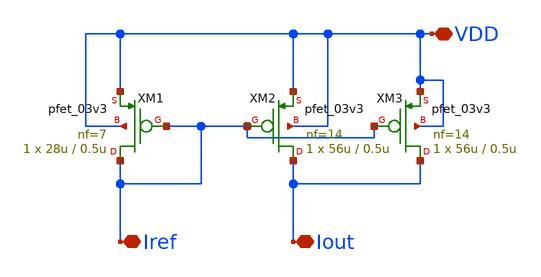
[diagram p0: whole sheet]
** sch_path: designs/mirrors/schematic/pmos_mirror.sch
**.subckt pmos_mirror VDD Iref Iout
*.iopin VDD
*.iopin Iref
*.iopin Iout
XM1 Iref Iref VDD VDD pfet_03v3 L=0.5u W=28u nf=7 ad='int((nf+1)/2) * W/nf * 0.18u' as='int((nf+2)/2) * W/nf * 0.18u'
+ pd='2*int((nf+1)/2) * (W/nf + 0.18u)' ps='2*int((nf+2)/2) * (W/nf + 0.18u)' nrd='0.18u / W' nrs='0.18u / W'
+ sa=0 sb=0 sd=0 m=1
XM2 Iout Iref VDD VDD pfet_03v3 L=0.5u W=56u nf=14 ad='int((nf+1)/2) * W/nf * 0.18u' as='int((nf+2)/2) * W/nf * 0.18u'
+ pd='2*int((nf+1)/2) * (W/nf + 0.18u)' ps='2*int((nf+2)/2) * (W/nf + 0.18u)' nrd='0.18u / W' nrs='0.18u / W'
+ sa=0 sb=0 sd=0 m=1
XM3 Iout Iref VDD VDD pfet_03v3 L=0.5u W=56u nf=14 ad='int((nf+1)/2) * W/nf * 0.18u' as='int((nf+2)/2) * W/nf * 0.18u'
+ pd='2*int((nf+1)/2) * (W/nf + 0.18u)' ps='2*int((nf+2)/2) * (W/nf + 0.18u)' nrd='0.18u / W' nrs='0.18u / W'
+ sa=0 sb=0 sd=0 m=1
**.ends
.end
